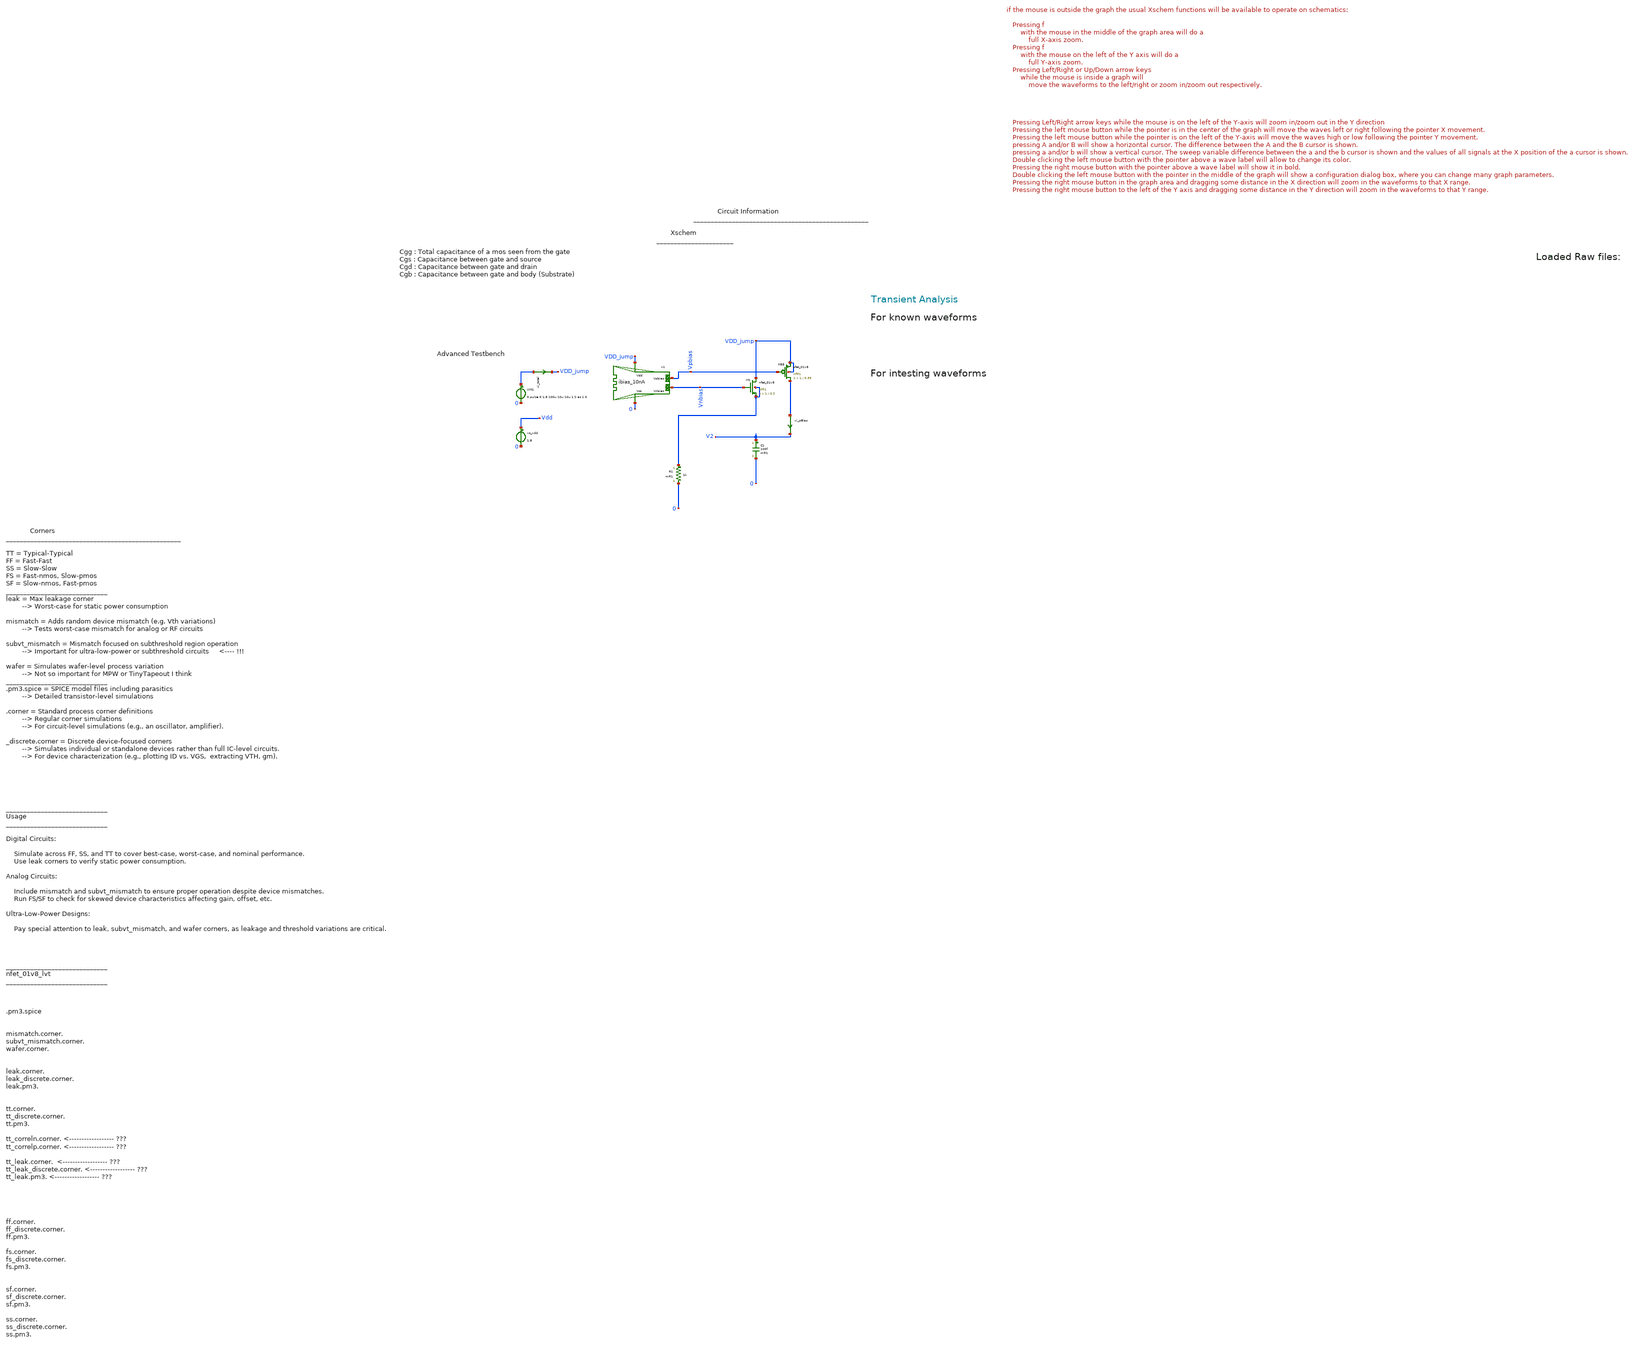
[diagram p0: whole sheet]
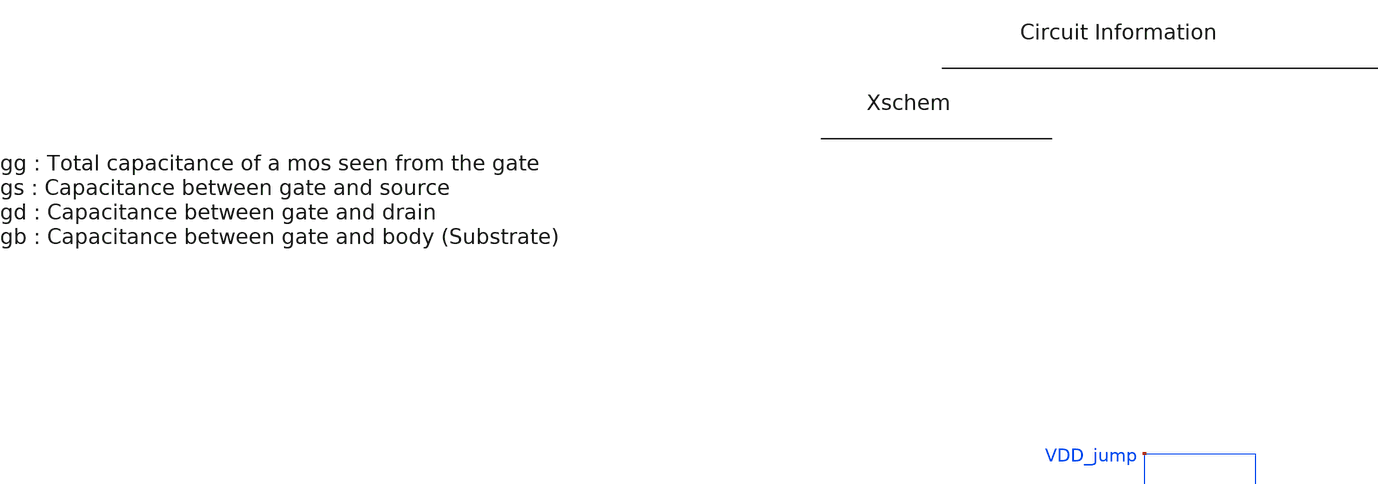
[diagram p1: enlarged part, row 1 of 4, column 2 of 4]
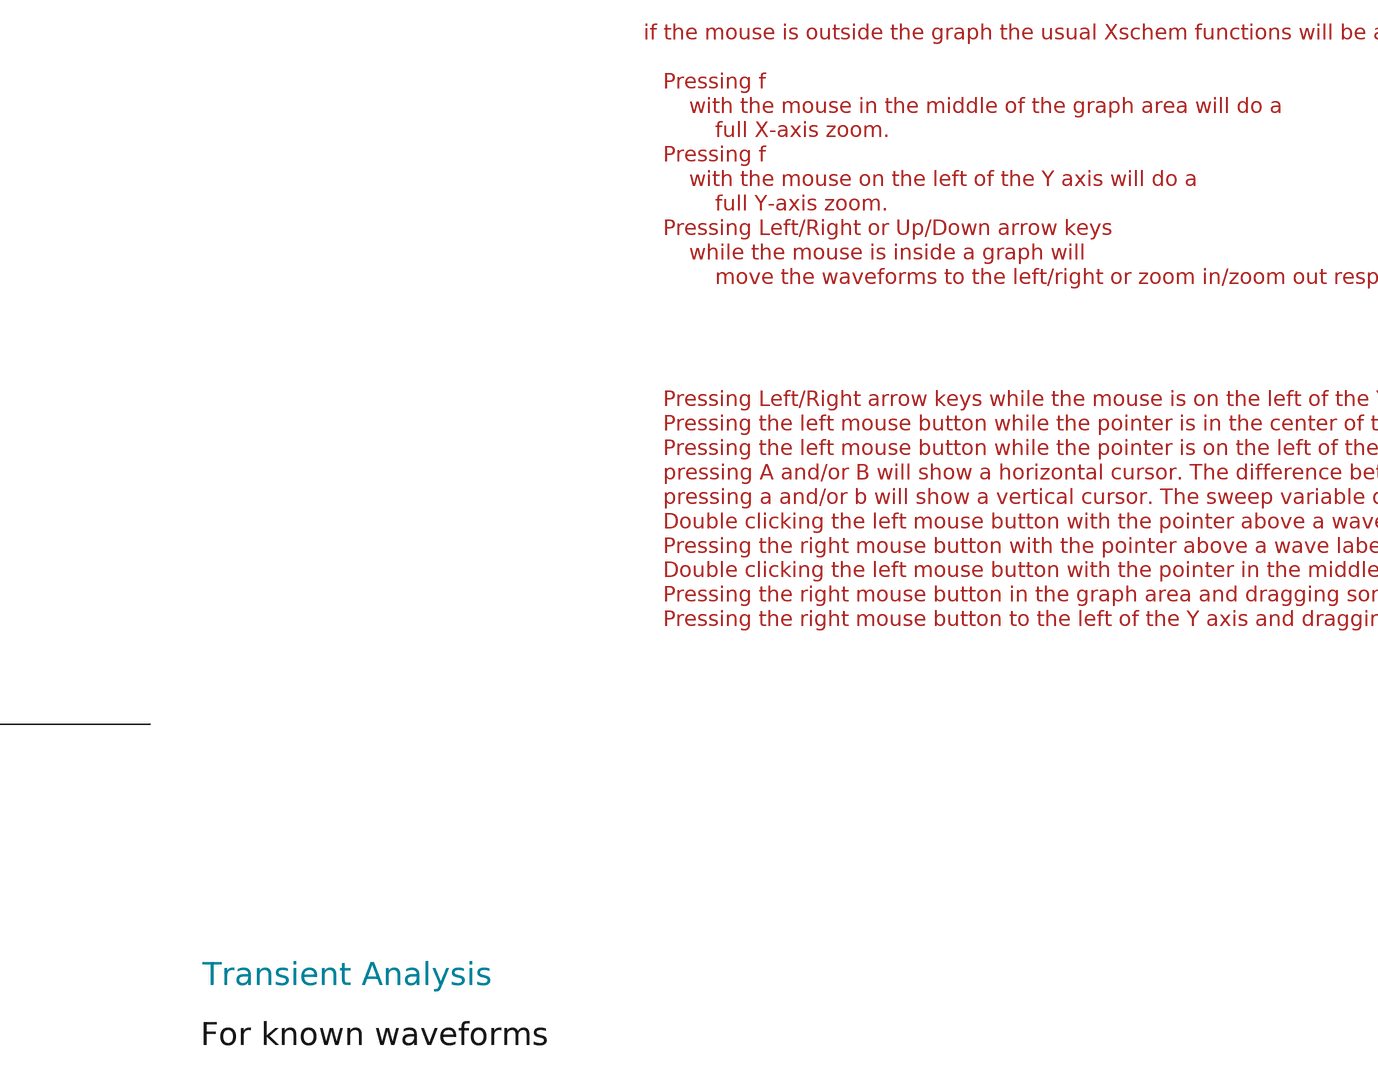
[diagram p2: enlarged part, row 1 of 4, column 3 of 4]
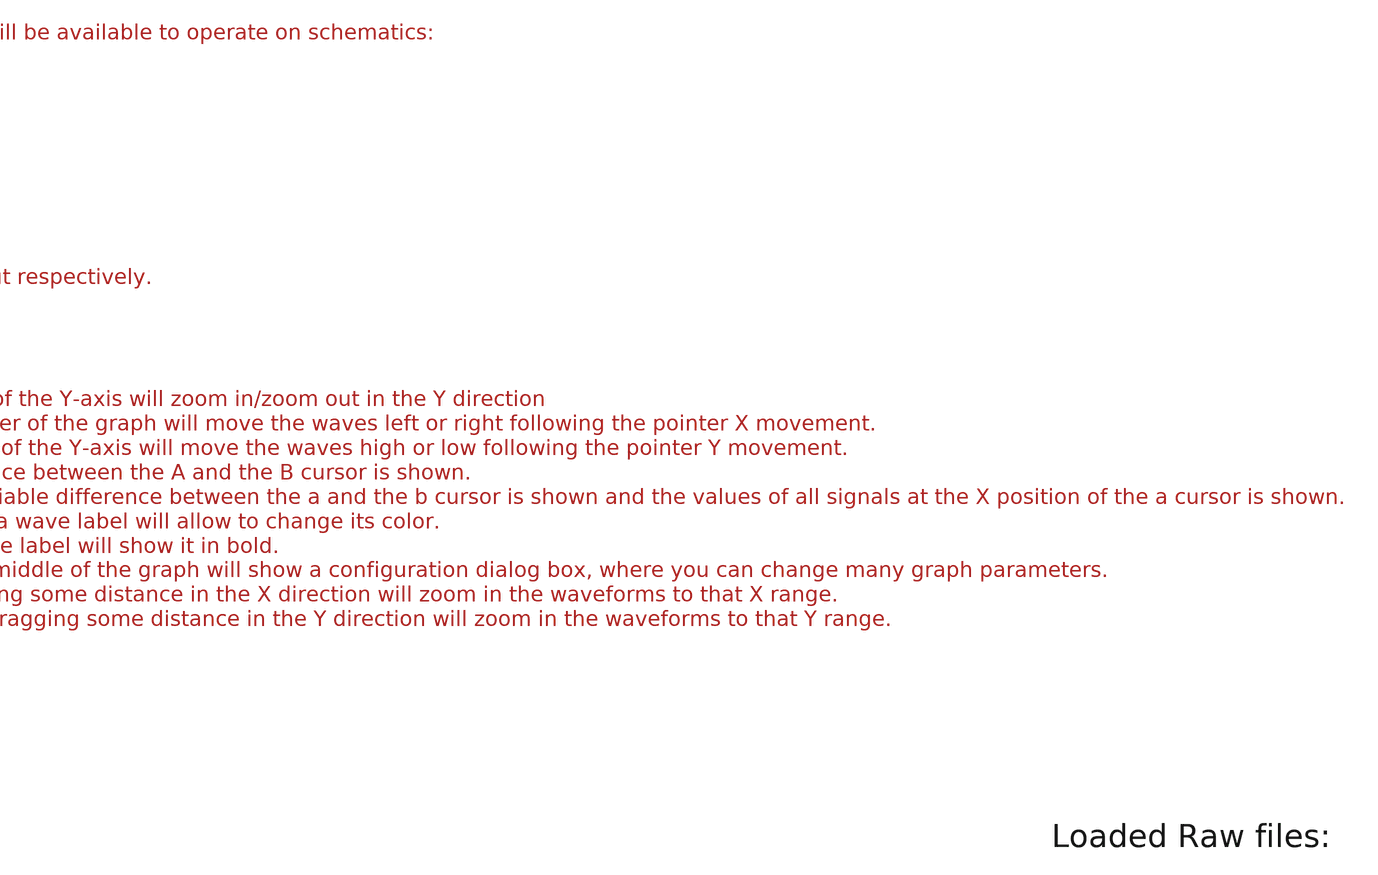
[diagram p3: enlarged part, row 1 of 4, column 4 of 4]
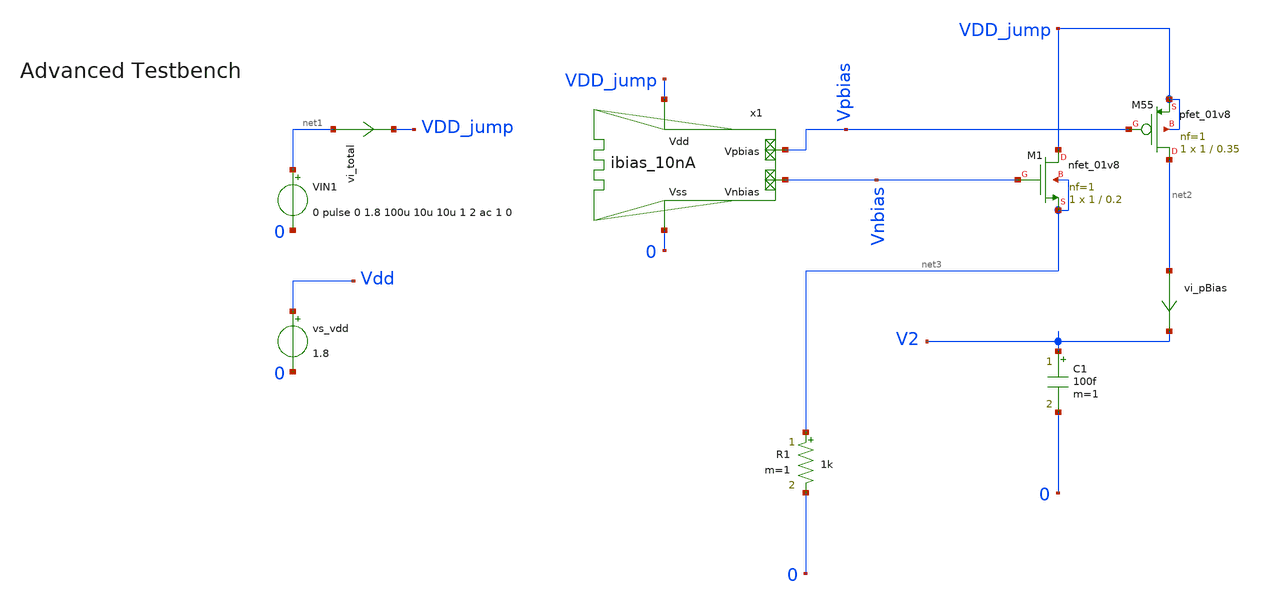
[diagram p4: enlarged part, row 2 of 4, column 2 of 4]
** sch_path: tt10-hdl/tt_um_test_commit/xschem/T0/mosCap/pCap_tb.sch
* Copyright (C) 1998-2024 Stefan Frederik Schippers
* This program is free software; you can redistribute it and/or modify
* it under the terms of the GNU General Public License as published by
* the Free Software Foundation; either version 2 of the License, or
* (at your option) any later version.
* This program is distributed in the hope that it will be useful,
* but WITHOUT ANY WARRANTY; without even the implied warranty of
* MERCHANTABILITY or FITNESS FOR A PARTICULAR PURPOSE.  See the
* GNU General Public License for more details.
* You should have received a copy of the GNU General Public License
* along with this program; if not, write to the Free Software
**.subckt pCap_tb
VIN1 net1 0 0 pulse 0 1.8 100u 10u 10u 1 2 ac 1 0
vi_total net1 VDD_jump 0
.save i(vi_total)
vs_vdd Vdd 0 1.8
XM1 VDD_jump Vnbias net3 net3 sky130_fd_pr__nfet_01v8 L=0.2 W=1 nf=1 ad='int((1 + 1)/2) * 1 / 1 * 0.29'
+ as='int((1 + 2)/2) * 1 / 1 * 0.29' pd='2*int((1 + 1)/2) * (1 / 1 + 0.29)' ps='2*int((1 + 2)/2) * (1 / 1 + 0.29)'
+ nrd='0.29 / 1 ' nrs='0.29 / 1 ' sa=0 sb=0 sd=0 mult=1 m=1
x1 VDD_jump 0 Vnbias Vpbias ibias_10nA
XM55 net2 Vpbias VDD_jump VDD_jump sky130_fd_pr__pfet_01v8 L=0.35 W=1 nf=1 ad='int((nf+1)/2) * W/nf * 0.29'
+ as='int((nf+2)/2) * W/nf * 0.29' pd='2*int((nf+1)/2) * (W/nf + 0.29)' ps='2*int((nf+2)/2) * (W/nf + 0.29)'
+ nrd='0.29 / W' nrs='0.29 / W' sa=0 sb=0 sd=0 mult=1 m=1
vi_pBias net2 V2 0
.save i(vi_pbias)
C1 V2 0 100f m=1
R1 net3 0 1k m=1
**** begin user architecture code



.temp 30

*.option gmin=5n
*.option scale=1e-6
.option wnflag=1

.save all
.control



  *dc v_dev_vds 0 1.8 0.005 v_dev_vgs 0 1.8 0.2
  *write nmos_tb.raw




  tran 0.1u 200u
  write nmos_tb_tran.raw

  op
  set appendwrite
  write nmos_tb_tran.raw






  *quit 0




.endc





** opencircuitdesign pdks install
.lib $::SKYWATER_MODELS/sky130.lib.spice tt
.include $::SKYWATER_STDCELLS/sky130_fd_sc_hd.spice


**** end user architecture code
**.ends

* expanding   symbol:  T2/biasGen/A_tt10_10nA/ibias_10nA.sym # of pins=4
** sym_path: tt10-hdl/tt_um_test_commit/xschem/T2/biasGen/A_tt10_10nA/ibias_10nA.sym
** sch_path: tt10-hdl/tt_um_test_commit/xschem/T2/biasGen/A_tt10_10nA/ibias_10nA.sch
.subckt ibias_10nA Vdd Vss Vnbias Vpbias
*.ipin Vdd
*.ipin Vss
*.opin Vnbias
*.opin Vpbias
XM3 Vpbias Vpbias Vdd Vdd sky130_fd_pr__pfet_01v8 L=0.35 W=0.5 nf=1 ad='int((nf+1)/2) * W/nf * 0.29'
+ as='int((nf+2)/2) * W/nf * 0.29' pd='2*int((nf+1)/2) * (W/nf + 0.29)' ps='2*int((nf+2)/2) * (W/nf + 0.29)'
+ nrd='0.29 / W' nrs='0.29 / W' sa=0 sb=0 sd=0 mult=1 m=1
XM4 Vnbias Vpbias Vdd Vdd sky130_fd_pr__pfet_01v8 L=0.35 W=0.5 nf=1 ad='int((nf+1)/2) * W/nf * 0.29'
+ as='int((nf+2)/2) * W/nf * 0.29' pd='2*int((nf+1)/2) * (W/nf + 0.29)' ps='2*int((nf+2)/2) * (W/nf + 0.29)'
+ nrd='0.29 / W' nrs='0.29 / W' sa=0 sb=0 sd=0 mult=1 m=1
XM5 net2 Vpbias Vdd Vdd sky130_fd_pr__pfet_01v8 L=0.35 W=1 nf=1 ad='int((nf+1)/2) * W/nf * 0.29' as='int((nf+2)/2) * W/nf * 0.29'
+ pd='2*int((nf+1)/2) * (W/nf + 0.29)' ps='2*int((nf+2)/2) * (W/nf + 0.29)' nrd='0.29 / W' nrs='0.29 / W'
+ sa=0 sb=0 sd=0 mult=1 m=1
XM1 Vpbias Vnbias net1 Vss sky130_fd_pr__nfet_01v8 L=0.2 W=0.5 nf=1 ad='int((1 + 1)/2) * 0.5 / 1 * 0.29'
+ as='int((1 + 2)/2) * 0.5 / 1 * 0.29' pd='2*int((1 + 1)/2) * (0.5 / 1 + 0.29)' ps='2*int((1 + 2)/2) * (0.5 / 1 + 0.29)'
+ nrd='0.29 / 0.5 ' nrs='0.29 / 0.5 ' sa=0 sb=0 sd=0 mult=1 m=1
XM2 Vnbias Vnbias Vss Vss sky130_fd_pr__nfet_01v8 L=0.2 W=0.5 nf=1 ad='int((1 + 1)/2) * 0.5 / 1 * 0.29'
+ as='int((1 + 2)/2) * 0.5 / 1 * 0.29' pd='2*int((1 + 1)/2) * (0.5 / 1 + 0.29)' ps='2*int((1 + 2)/2) * (0.5 / 1 + 0.29)'
+ nrd='0.29 / 0.5 ' nrs='0.29 / 0.5 ' sa=0 sb=0 sd=0 mult=1 m=1
XM6 net2 net2 net1 Vss sky130_fd_pr__nfet_01v8 L=0.2 W=1 nf=1 ad='int((1 + 1)/2) * 1 / 1 * 0.29' as='int((1 + 2)/2) * 1 / 1 * 0.29'
+ pd='2*int((1 + 1)/2) * (1 / 1 + 0.29)' ps='2*int((1 + 2)/2) * (1 / 1 + 0.29)' nrd='0.29 / 1 ' nrs='0.29 / 1 '
+ sa=0 sb=0 sd=0 mult=1 m=1
XM7 net1 net2 Vss Vss sky130_fd_pr__nfet_01v8 L=1 W=1 nf=1 ad='int((1 + 1)/2) * 1 / 1 * 0.29' as='int((1 + 2)/2) * 1 / 1 * 0.29'
+ pd='2*int((1 + 1)/2) * (1 / 1 + 0.29)' ps='2*int((1 + 2)/2) * (1 / 1 + 0.29)' nrd='0.29 / 1 ' nrs='0.29 / 1 '
+ sa=0 sb=0 sd=0 mult=1 m=1
.ends

.end
